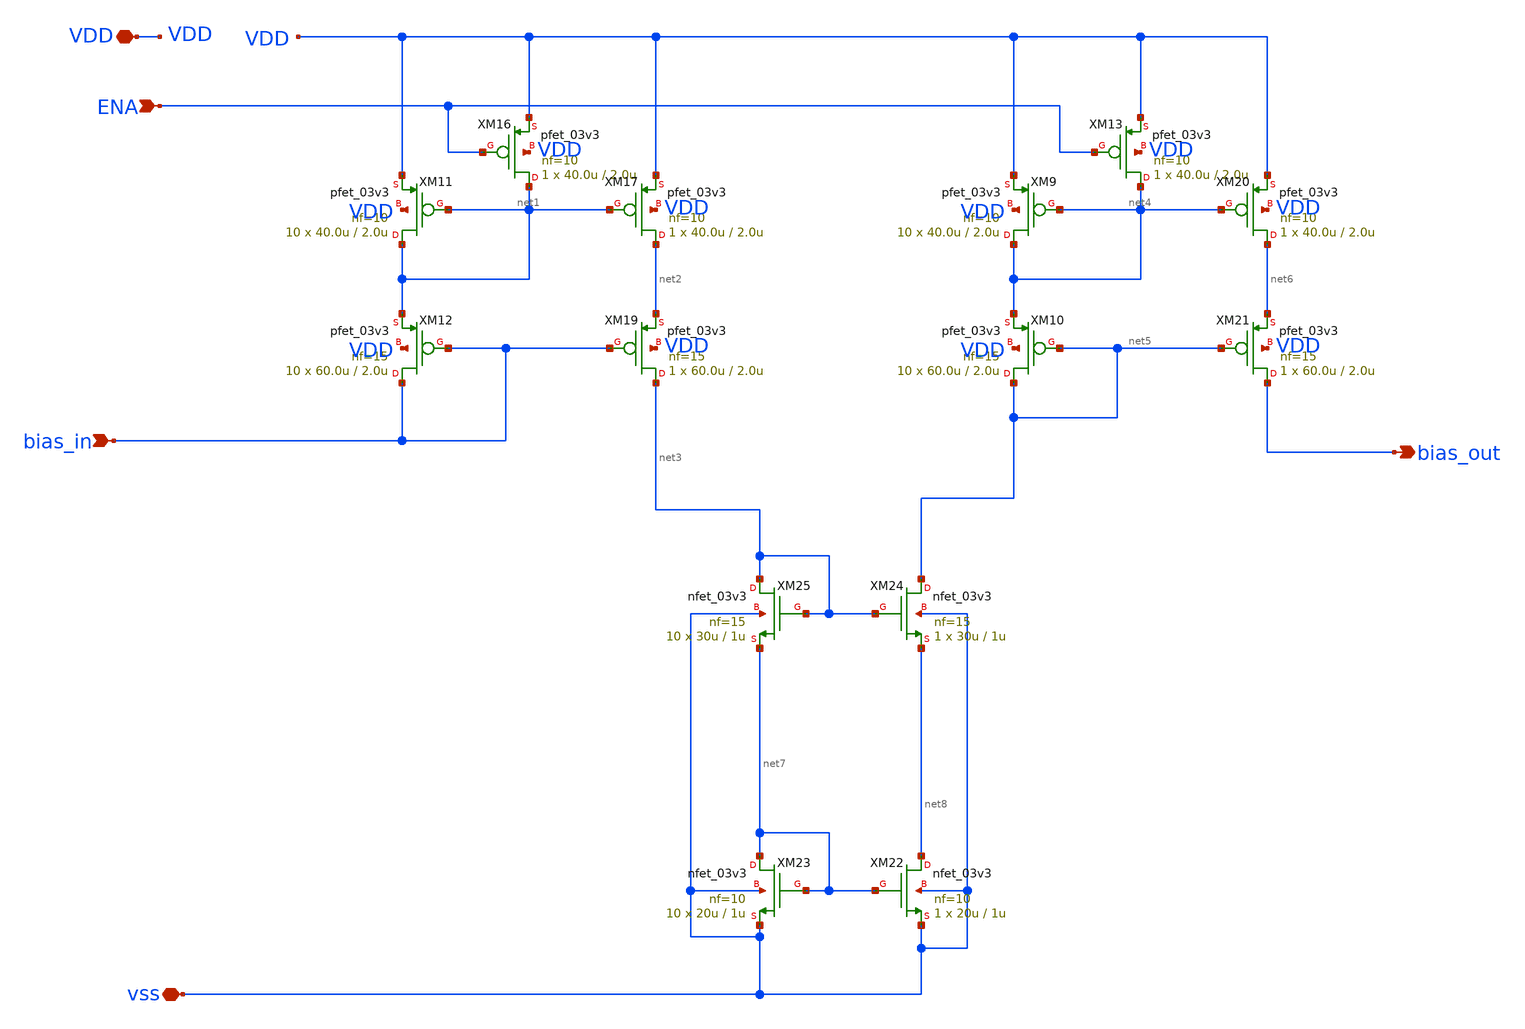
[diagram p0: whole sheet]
** sch_path: blocks/composite/regulated_cascoded_cmirror/xschem/bias.sch
**.subckt bias vss VDD ENA bias_in bias_out
*.iopin vss
*.iopin VDD
*.ipin ENA
*.ipin bias_in
*.opin bias_out
XM11 net1 net1 VDD VDD pfet_03v3 L=2.0u W=40.0u nf=10 ad='int((nf+1)/2) * W/nf * 0.18u' as='int((nf+2)/2) * W/nf * 0.18u'
+ pd='2*int((nf+1)/2) * (W/nf + 0.18u)' ps='2*int((nf+2)/2) * (W/nf + 0.18u)' nrd='0.18u / W' nrs='0.18u / W'
+ sa=0 sb=0 sd=0 m=10
XM12 bias_in bias_in net1 VDD pfet_03v3 L=2.0u W=60.0u nf=15 ad='int((nf+1)/2) * W/nf * 0.18u' as='int((nf+2)/2) * W/nf * 0.18u'
+ pd='2*int((nf+1)/2) * (W/nf + 0.18u)' ps='2*int((nf+2)/2) * (W/nf + 0.18u)' nrd='0.18u / W' nrs='0.18u / W'
+ sa=0 sb=0 sd=0 m=10
XM16 net1 ENA VDD VDD pfet_03v3 L=2.0u W=40.0u nf=10 ad='int((nf+1)/2) * W/nf * 0.18u' as='int((nf+2)/2) * W/nf * 0.18u'
+ pd='2*int((nf+1)/2) * (W/nf + 0.18u)' ps='2*int((nf+2)/2) * (W/nf + 0.18u)' nrd='0.18u / W' nrs='0.18u / W'
+ sa=0 sb=0 sd=0 m=1
XM17 net2 net1 VDD VDD pfet_03v3 L=2.0u W=40.0u nf=10 ad='int((nf+1)/2) * W/nf * 0.18u' as='int((nf+2)/2) * W/nf * 0.18u'
+ pd='2*int((nf+1)/2) * (W/nf + 0.18u)' ps='2*int((nf+2)/2) * (W/nf + 0.18u)' nrd='0.18u / W' nrs='0.18u / W'
+ sa=0 sb=0 sd=0 m=1
XM19 net3 bias_in net2 VDD pfet_03v3 L=2.0u W=60.0u nf=15 ad='int((nf+1)/2) * W/nf * 0.18u' as='int((nf+2)/2) * W/nf * 0.18u'
+ pd='2*int((nf+1)/2) * (W/nf + 0.18u)' ps='2*int((nf+2)/2) * (W/nf + 0.18u)' nrd='0.18u / W' nrs='0.18u / W'
+ sa=0 sb=0 sd=0 m=1
XM9 net4 net4 VDD VDD pfet_03v3 L=2.0u W=40.0u nf=10 ad='int((nf+1)/2) * W/nf * 0.18u' as='int((nf+2)/2) * W/nf * 0.18u'
+ pd='2*int((nf+1)/2) * (W/nf + 0.18u)' ps='2*int((nf+2)/2) * (W/nf + 0.18u)' nrd='0.18u / W' nrs='0.18u / W'
+ sa=0 sb=0 sd=0 m=10
XM10 net5 net5 net4 VDD pfet_03v3 L=2.0u W=60.0u nf=15 ad='int((nf+1)/2) * W/nf * 0.18u' as='int((nf+2)/2) * W/nf * 0.18u'
+ pd='2*int((nf+1)/2) * (W/nf + 0.18u)' ps='2*int((nf+2)/2) * (W/nf + 0.18u)' nrd='0.18u / W' nrs='0.18u / W'
+ sa=0 sb=0 sd=0 m=10
XM13 net4 ENA VDD VDD pfet_03v3 L=2.0u W=40.0u nf=10 ad='int((nf+1)/2) * W/nf * 0.18u' as='int((nf+2)/2) * W/nf * 0.18u'
+ pd='2*int((nf+1)/2) * (W/nf + 0.18u)' ps='2*int((nf+2)/2) * (W/nf + 0.18u)' nrd='0.18u / W' nrs='0.18u / W'
+ sa=0 sb=0 sd=0 m=1
XM20 net6 net4 VDD VDD pfet_03v3 L=2.0u W=40.0u nf=10 ad='int((nf+1)/2) * W/nf * 0.18u' as='int((nf+2)/2) * W/nf * 0.18u'
+ pd='2*int((nf+1)/2) * (W/nf + 0.18u)' ps='2*int((nf+2)/2) * (W/nf + 0.18u)' nrd='0.18u / W' nrs='0.18u / W'
+ sa=0 sb=0 sd=0 m=1
XM21 bias_out net5 net6 VDD pfet_03v3 L=2.0u W=60.0u nf=15 ad='int((nf+1)/2) * W/nf * 0.18u' as='int((nf+2)/2) * W/nf * 0.18u'
+ pd='2*int((nf+1)/2) * (W/nf + 0.18u)' ps='2*int((nf+2)/2) * (W/nf + 0.18u)' nrd='0.18u / W' nrs='0.18u / W'
+ sa=0 sb=0 sd=0 m=1
XM22 net8 net7 vss vss nfet_03v3 L=1u W=20u nf=10 ad='int((nf+1)/2) * W/nf * 0.18u' as='int((nf+2)/2) * W/nf * 0.18u'
+ pd='2*int((nf+1)/2) * (W/nf + 0.18u)' ps='2*int((nf+2)/2) * (W/nf + 0.18u)' nrd='0.18u / W' nrs='0.18u / W'
+ sa=0 sb=0 sd=0 m=1
XM23 net7 net7 vss vss nfet_03v3 L=1u W=20u nf=10 ad='int((nf+1)/2) * W/nf * 0.18u' as='int((nf+2)/2) * W/nf * 0.18u'
+ pd='2*int((nf+1)/2) * (W/nf + 0.18u)' ps='2*int((nf+2)/2) * (W/nf + 0.18u)' nrd='0.18u / W' nrs='0.18u / W'
+ sa=0 sb=0 sd=0 m=10
XM24 net5 net3 net8 vss nfet_03v3 L=1u W=30u nf=15 ad='int((nf+1)/2) * W/nf * 0.18u' as='int((nf+2)/2) * W/nf * 0.18u'
+ pd='2*int((nf+1)/2) * (W/nf + 0.18u)' ps='2*int((nf+2)/2) * (W/nf + 0.18u)' nrd='0.18u / W' nrs='0.18u / W'
+ sa=0 sb=0 sd=0 m=1
XM25 net3 net3 net7 vss nfet_03v3 L=1u W=30u nf=15 ad='int((nf+1)/2) * W/nf * 0.18u' as='int((nf+2)/2) * W/nf * 0.18u'
+ pd='2*int((nf+1)/2) * (W/nf + 0.18u)' ps='2*int((nf+2)/2) * (W/nf + 0.18u)' nrd='0.18u / W' nrs='0.18u / W'
+ sa=0 sb=0 sd=0 m=10
**.ends
.end
